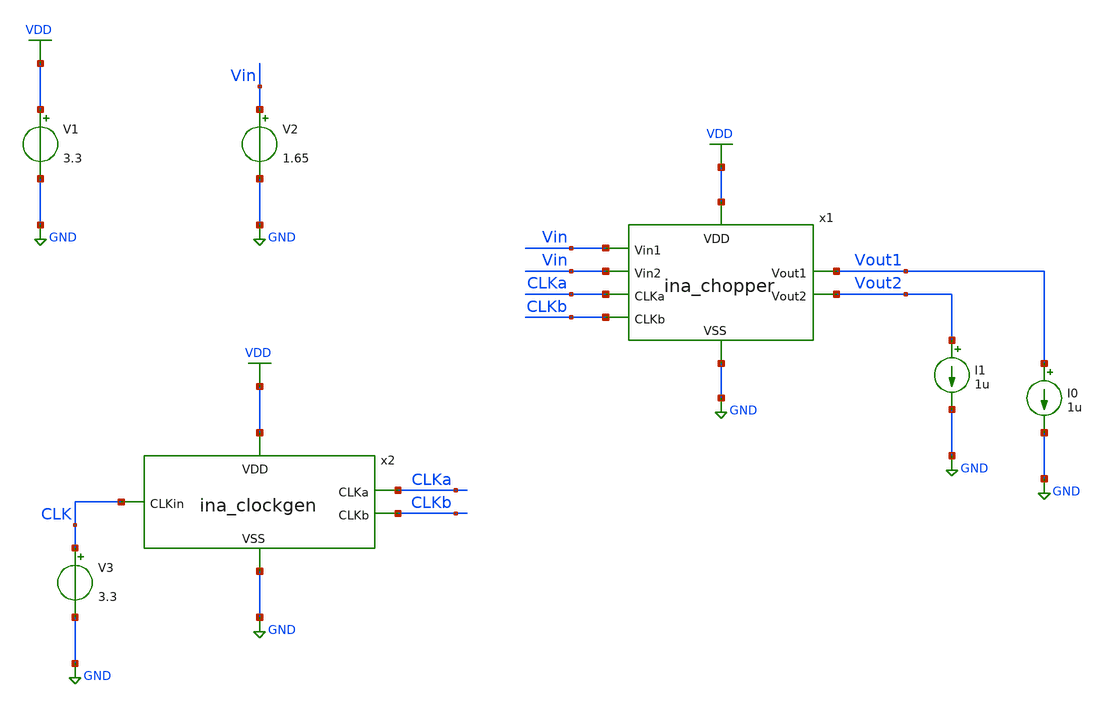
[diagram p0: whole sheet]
** sch_path: designs/libs/tb_ina/tb_ina_chopper_dc/tb_ina_chopper_dc.sch
**.subckt tb_ina_chopper_dc
V1 VDD GND 3.3
V2 Vin GND 1.65
V3 CLK GND 3.3
x1 Vout2 Vin VDD GND CLKb CLKa Vout1 Vin ina_chopper
x2 VDD CLK CLKa CLKb GND ina_clockgen
I0 Vout1 GND 1u
I1 Vout2 GND 1u
**** begin user architecture code

.include $::180MCU_MODELS/design.ngspice
.lib $::180MCU_MODELS/sm141064.ngspice typical
.lib $::180MCU_MODELS/sm141064.ngspice cap_mim
.lib $::180MCU_MODELS/sm141064.ngspice moscap_typical
.lib $::180MCU_MODELS/sm141064.ngspice mimcap_typical
.lib $::180MCU_MODELS/sm141064.ngspice res_typical
* .lib $::180MCU_MODELS/sm141064.ngspice res_statistical
* ngspice commands




.control
save all

set color0 = white

*************************************
** INPUT PARAMETERS
*************************************

let Vdd  = 3.3
let Itest = 1u

*************************************
** SOURCES
*************************************

alter @V1[DC] = $&Vdd
alter @V2[DC] = 0
alter @V3[DC] = $&Vdd
alter @I0[DC] = $&Itest
alter @I1[DC] = $&Itest

*************************************
** DC SWEEP SIMULATION
*************************************

dc V2 0 3.3 0.001

*************************************
** PLOTS
*************************************

setplot dc1
let vout1 = v(Vout1)
let vout2 = v(Vout2)
let vin = v(Vin)
let Ron1 = (vin - vout1)/$&Itest
let Ron2 = (vin - vout2)/$&Itest
plot Ron1 Ron2

*************************************
** SAVE
*************************************

write tb_ina_chopper_dc.raw

.endc
* ngspice commands



**** end user architecture code
**.ends

* expanding   symbol:  libs/core_ina/ina_chopper/ina_chopper.sym # of pins=8
** sym_path: designs/libs/core_ina/ina_chopper/ina_chopper.sym
** sch_path: designs/libs/core_ina/ina_chopper/ina_chopper.sch
.subckt ina_chopper Vout2 Vin1 VDD VSS CLKb CLKa Vout1 Vin2
*.ipin Vin1
*.ipin Vin2
*.ipin CLKb
*.opin Vout2
*.ipin CLKa
*.opin Vout1
*.ipin VDD
*.ipin VSS
XM1 Vout1 CLKa Vin1 VSS nfet_03v3 L=0.28u W=2u nf=1 ad='int((nf+1)/2) * W/nf * 0.18u' as='int((nf+2)/2) * W/nf * 0.18u'
+ pd='2*int((nf+1)/2) * (W/nf + 0.18u)' ps='2*int((nf+2)/2) * (W/nf + 0.18u)' nrd='0.18u / W' nrs='0.18u / W'
+ sa=0 sb=0 sd=0 m=1
XM2 Vout1 CLKb Vin1 VDD pfet_03v3 L=0.28u W=2u nf=1 ad='int((nf+1)/2) * W/nf * 0.18u' as='int((nf+2)/2) * W/nf * 0.18u'
+ pd='2*int((nf+1)/2) * (W/nf + 0.18u)' ps='2*int((nf+2)/2) * (W/nf + 0.18u)' nrd='0.18u / W' nrs='0.18u / W'
+ sa=0 sb=0 sd=0 m=2
XM3 Vout2 CLKb Vin1 VSS nfet_03v3 L=0.28u W=2u nf=1 ad='int((nf+1)/2) * W/nf * 0.18u' as='int((nf+2)/2) * W/nf * 0.18u'
+ pd='2*int((nf+1)/2) * (W/nf + 0.18u)' ps='2*int((nf+2)/2) * (W/nf + 0.18u)' nrd='0.18u / W' nrs='0.18u / W'
+ sa=0 sb=0 sd=0 m=1
XM4 Vout2 CLKa Vin1 VDD pfet_03v3 L=0.28u W=2u nf=1 ad='int((nf+1)/2) * W/nf * 0.18u' as='int((nf+2)/2) * W/nf * 0.18u'
+ pd='2*int((nf+1)/2) * (W/nf + 0.18u)' ps='2*int((nf+2)/2) * (W/nf + 0.18u)' nrd='0.18u / W' nrs='0.18u / W'
+ sa=0 sb=0 sd=0 m=2
XM5 Vin2 CLKa Vout2 VSS nfet_03v3 L=0.28u W=2u nf=1 ad='int((nf+1)/2) * W/nf * 0.18u' as='int((nf+2)/2) * W/nf * 0.18u'
+ pd='2*int((nf+1)/2) * (W/nf + 0.18u)' ps='2*int((nf+2)/2) * (W/nf + 0.18u)' nrd='0.18u / W' nrs='0.18u / W'
+ sa=0 sb=0 sd=0 m=1
XM6 Vin2 CLKb Vout2 VDD pfet_03v3 L=0.28u W=2u nf=1 ad='int((nf+1)/2) * W/nf * 0.18u' as='int((nf+2)/2) * W/nf * 0.18u'
+ pd='2*int((nf+1)/2) * (W/nf + 0.18u)' ps='2*int((nf+2)/2) * (W/nf + 0.18u)' nrd='0.18u / W' nrs='0.18u / W'
+ sa=0 sb=0 sd=0 m=2
XM7 Vin2 CLKb Vout1 VSS nfet_03v3 L=0.28u W=2u nf=1 ad='int((nf+1)/2) * W/nf * 0.18u' as='int((nf+2)/2) * W/nf * 0.18u'
+ pd='2*int((nf+1)/2) * (W/nf + 0.18u)' ps='2*int((nf+2)/2) * (W/nf + 0.18u)' nrd='0.18u / W' nrs='0.18u / W'
+ sa=0 sb=0 sd=0 m=1
XM8 Vin2 CLKa Vout1 VDD pfet_03v3 L=0.28u W=2u nf=1 ad='int((nf+1)/2) * W/nf * 0.18u' as='int((nf+2)/2) * W/nf * 0.18u'
+ pd='2*int((nf+1)/2) * (W/nf + 0.18u)' ps='2*int((nf+2)/2) * (W/nf + 0.18u)' nrd='0.18u / W' nrs='0.18u / W'
+ sa=0 sb=0 sd=0 m=2
XM9 Vout1 CLKb Vout1 VSS nfet_03v3 L=0.28u W=1u nf=1 ad='int((nf+1)/2) * W/nf * 0.18u' as='int((nf+2)/2) * W/nf * 0.18u'
+ pd='2*int((nf+1)/2) * (W/nf + 0.18u)' ps='2*int((nf+2)/2) * (W/nf + 0.18u)' nrd='0.18u / W' nrs='0.18u / W'
+ sa=0 sb=0 sd=0 m=1
XM10 Vout1 CLKa Vout1 VDD pfet_03v3 L=0.28u W=1u nf=1 ad='int((nf+1)/2) * W/nf * 0.18u' as='int((nf+2)/2) * W/nf * 0.18u'
+ pd='2*int((nf+1)/2) * (W/nf + 0.18u)' ps='2*int((nf+2)/2) * (W/nf + 0.18u)' nrd='0.18u / W' nrs='0.18u / W'
+ sa=0 sb=0 sd=0 m=2
XM11 Vout2 CLKa Vout2 VSS nfet_03v3 L=0.28u W=1u nf=1 ad='int((nf+1)/2) * W/nf * 0.18u' as='int((nf+2)/2) * W/nf * 0.18u'
+ pd='2*int((nf+1)/2) * (W/nf + 0.18u)' ps='2*int((nf+2)/2) * (W/nf + 0.18u)' nrd='0.18u / W' nrs='0.18u / W'
+ sa=0 sb=0 sd=0 m=1
XM12 Vout2 CLKb Vout2 VDD pfet_03v3 L=0.28u W=1u nf=1 ad='int((nf+1)/2) * W/nf * 0.18u' as='int((nf+2)/2) * W/nf * 0.18u'
+ pd='2*int((nf+1)/2) * (W/nf + 0.18u)' ps='2*int((nf+2)/2) * (W/nf + 0.18u)' nrd='0.18u / W' nrs='0.18u / W'
+ sa=0 sb=0 sd=0 m=2
XM13 Vout2 CLKa Vout2 VDD pfet_03v3 L=0.28u W=1u nf=1 ad='int((nf+1)/2) * W/nf * 0.18u' as='int((nf+2)/2) * W/nf * 0.18u'
+ pd='2*int((nf+1)/2) * (W/nf + 0.18u)' ps='2*int((nf+2)/2) * (W/nf + 0.18u)' nrd='0.18u / W' nrs='0.18u / W'
+ sa=0 sb=0 sd=0 m=2
XM14 Vout2 CLKb Vout2 VSS nfet_03v3 L=0.28u W=1u nf=1 ad='int((nf+1)/2) * W/nf * 0.18u' as='int((nf+2)/2) * W/nf * 0.18u'
+ pd='2*int((nf+1)/2) * (W/nf + 0.18u)' ps='2*int((nf+2)/2) * (W/nf + 0.18u)' nrd='0.18u / W' nrs='0.18u / W'
+ sa=0 sb=0 sd=0 m=1
XM15 Vout1 CLKb Vout1 VDD pfet_03v3 L=0.28u W=1u nf=1 ad='int((nf+1)/2) * W/nf * 0.18u' as='int((nf+2)/2) * W/nf * 0.18u'
+ pd='2*int((nf+1)/2) * (W/nf + 0.18u)' ps='2*int((nf+2)/2) * (W/nf + 0.18u)' nrd='0.18u / W' nrs='0.18u / W'
+ sa=0 sb=0 sd=0 m=2
XM16 Vout1 CLKa Vout1 VSS nfet_03v3 L=0.28u W=1u nf=1 ad='int((nf+1)/2) * W/nf * 0.18u' as='int((nf+2)/2) * W/nf * 0.18u'
+ pd='2*int((nf+1)/2) * (W/nf + 0.18u)' ps='2*int((nf+2)/2) * (W/nf + 0.18u)' nrd='0.18u / W' nrs='0.18u / W'
+ sa=0 sb=0 sd=0 m=1
.ends


* expanding   symbol:  libs/core_ina/ina_clockgen/ina_clockgen.sym # of pins=5
** sym_path: designs/libs/core_ina/ina_clockgen/ina_clockgen.sym
** sch_path: designs/libs/core_ina/ina_clockgen/ina_clockgen.sch
.subckt ina_clockgen VDD CLKin CLKa CLKb VSS
*.ipin CLKin
*.ipin VDD
*.ipin VSS
*.opin CLKa
*.opin CLKb
x1 VDD net4 CLKin net1 VSS ina_nand
x2 VDD net6 net3 net2 VSS ina_nand
x3 VDD CLKin net2 VSS ina_inv
x4 VDD net4 net5 VSS ina_inv
x5 VDD net5 net3 VSS ina_inv
x6 VDD net3 CLKa VSS ina_inv
x7 VDD net6 net7 VSS ina_inv
x8 VDD net7 net1 VSS ina_inv
x9 VDD net1 CLKb VSS ina_inv
.ends


* expanding   symbol:  libs/core_ina/ina_nand/ina_nand.sym # of pins=5
** sym_path: designs/libs/core_ina/ina_nand/ina_nand.sym
** sch_path: designs/libs/core_ina/ina_nand/ina_nand.sch
.subckt ina_nand VDD Vout Vin1 Vin2 VSS
*.ipin VDD
*.ipin Vin1
*.ipin Vin2
*.ipin VSS
*.opin Vout
XMN1 Vout Vin1 VDD VDD pfet_03v3 L=0.28u W=2u nf=1 ad='int((nf+1)/2) * W/nf * 0.18u' as='int((nf+2)/2) * W/nf * 0.18u'
+ pd='2*int((nf+1)/2) * (W/nf + 0.18u)' ps='2*int((nf+2)/2) * (W/nf + 0.18u)' nrd='0.18u / W' nrs='0.18u / W'
+ sa=0 sb=0 sd=0 m=1
XMN2 Vout Vin2 VDD VDD pfet_03v3 L=0.28u W=2u nf=1 ad='int((nf+1)/2) * W/nf * 0.18u' as='int((nf+2)/2) * W/nf * 0.18u'
+ pd='2*int((nf+1)/2) * (W/nf + 0.18u)' ps='2*int((nf+2)/2) * (W/nf + 0.18u)' nrd='0.18u / W' nrs='0.18u / W'
+ sa=0 sb=0 sd=0 m=1
XMN3 Vout Vin1 net1 VSS nfet_03v3 L=0.28u W=2u nf=1 ad='int((nf+1)/2) * W/nf * 0.18u' as='int((nf+2)/2) * W/nf * 0.18u'
+ pd='2*int((nf+1)/2) * (W/nf + 0.18u)' ps='2*int((nf+2)/2) * (W/nf + 0.18u)' nrd='0.18u / W' nrs='0.18u / W'
+ sa=0 sb=0 sd=0 m=1
XMN4 net1 Vin2 VSS VSS nfet_03v3 L=0.28u W=2u nf=1 ad='int((nf+1)/2) * W/nf * 0.18u' as='int((nf+2)/2) * W/nf * 0.18u'
+ pd='2*int((nf+1)/2) * (W/nf + 0.18u)' ps='2*int((nf+2)/2) * (W/nf + 0.18u)' nrd='0.18u / W' nrs='0.18u / W'
+ sa=0 sb=0 sd=0 m=1
.ends


* expanding   symbol:  libs/core_ina/ina_inv/ina_inv.sym # of pins=4
** sym_path: designs/libs/core_ina/ina_inv/ina_inv.sym
** sch_path: designs/libs/core_ina/ina_inv/ina_inv.sch
.subckt ina_inv VDD Vin Vout VSS
*.ipin VDD
*.ipin VSS
*.ipin Vin
*.opin Vout
XMI1 Vout Vin VDD VDD pfet_03v3 L=0.28u W=2u nf=1 ad='int((nf+1)/2) * W/nf * 0.18u' as='int((nf+2)/2) * W/nf * 0.18u'
+ pd='2*int((nf+1)/2) * (W/nf + 0.18u)' ps='2*int((nf+2)/2) * (W/nf + 0.18u)' nrd='0.18u / W' nrs='0.18u / W'
+ sa=0 sb=0 sd=0 m=1
XMI2 Vout Vin VSS VSS nfet_03v3 L=0.28u W=1u nf=1 ad='int((nf+1)/2) * W/nf * 0.18u' as='int((nf+2)/2) * W/nf * 0.18u'
+ pd='2*int((nf+1)/2) * (W/nf + 0.18u)' ps='2*int((nf+2)/2) * (W/nf + 0.18u)' nrd='0.18u / W' nrs='0.18u / W'
+ sa=0 sb=0 sd=0 m=1
.ends

.GLOBAL GND
.GLOBAL VDD
.end
